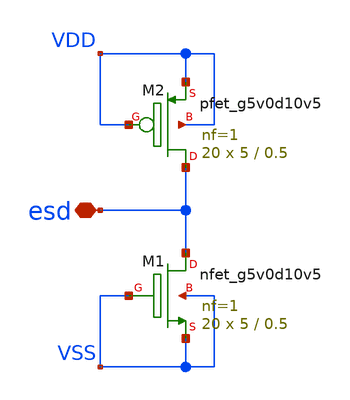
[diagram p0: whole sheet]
** sch_path: design/analog_modulator/schematic/esd_cell.sch
**.subckt esd_cell esd
*.iopin esd
XM1 esd VSS VSS VSS sky130_fd_pr__nfet_g5v0d10v5 L=0.5 W=5 nf=1 ad='int((nf+1)/2) * W/nf * 0.29' as='int((nf+2)/2) * W/nf * 0.29'
+ pd='2*int((nf+1)/2) * (W/nf + 0.29)' ps='2*int((nf+2)/2) * (W/nf + 0.29)' nrd='0.29 / W' nrs='0.29 / W'
+ sa=0 sb=0 sd=0 mult=20 m=20
XM2 esd VDD VDD VDD sky130_fd_pr__pfet_g5v0d10v5 L=0.5 W=5 nf=1 ad='int((nf+1)/2) * W/nf * 0.29' as='int((nf+2)/2) * W/nf * 0.29'
+ pd='2*int((nf+1)/2) * (W/nf + 0.29)' ps='2*int((nf+2)/2) * (W/nf + 0.29)' nrd='0.29 / W' nrs='0.29 / W'
+ sa=0 sb=0 sd=0 mult=20 m=20
**.ends
.end
